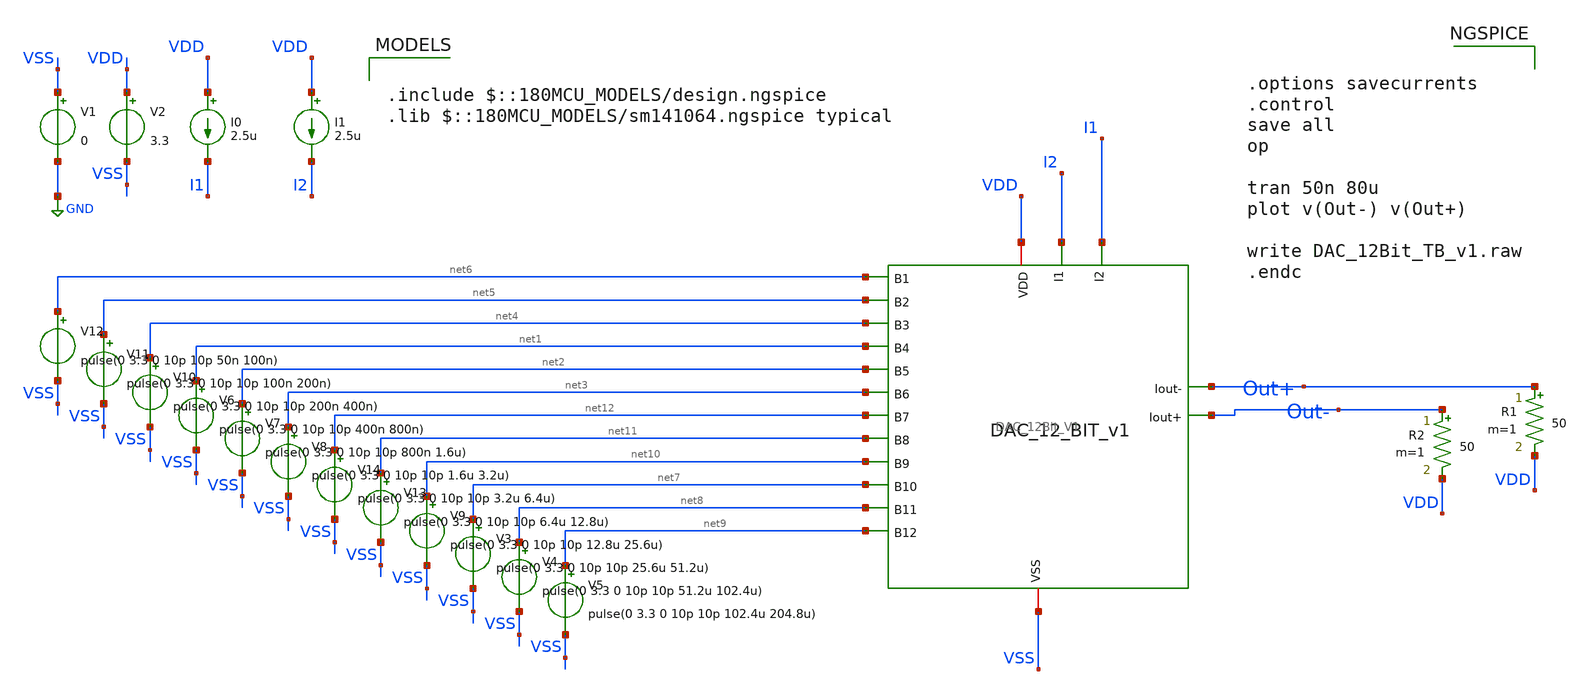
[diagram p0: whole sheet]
** sch_path: DAC_PAKISTAN_01/Pakistan1_Xschem/DAC_12Bit_TB_v1.sch
**.subckt DAC_12Bit_TB_v1
V1 VSS GND 0
V2 VDD VSS 3.3
V6 net1 VSS pulse(0 3.3 0 10p 10p 400n 800n)
V7 net2 VSS pulse(0 3.3 0 10p 10p 800n 1.6u)
V8 net3 VSS pulse(0 3.3 0 10p 10p 1.6u 3.2u)
V10 net4 VSS pulse(0 3.3 0 10p 10p 200n 400n)
V11 net5 VSS pulse(0 3.3 0 10p 10p 100n 200n)
V12 net6 VSS pulse(0 3.3 0 10p 10p 50n 100n)
I0 VDD I1 2.5u
V3 net7 VSS pulse(0 3.3 0 10p 10p 25.6u 51.2u)
V4 net8 VSS pulse(0 3.3 0 10p 10p 51.2u 102.4u)
V5 net9 VSS pulse(0 3.3 0 10p 10p 102.4u 204.8u)
V9 net10 VSS pulse(0 3.3 0 10p 10p 12.8u 25.6u)
V13 net11 VSS pulse(0 3.3 0 10p 10p 6.4u 12.8u)
V14 net12 VSS pulse(0 3.3 0 10p 10p 3.2u 6.4u)
I1 VDD I2 2.5u
R1 Out+ VDD 50 m=1
R2 Out- VDD 50 m=1
x1 net2 net10 VDD I2 net8 net6 net12 Out+ net4 net9 net7 net1 net11 Out- I1 net3 net5 VSS
+ DAC_12Bit_V1
**** begin user architecture code

.include $::180MCU_MODELS/design.ngspice
.lib $::180MCU_MODELS/sm141064.ngspice typical



.options savecurrents
.control
save all
op

tran 50n 80u
plot v(Out-) v(Out+)

write DAC_12Bit_TB_v1.raw
.endc


**** end user architecture code
**.ends
.GLOBAL GND
.end
